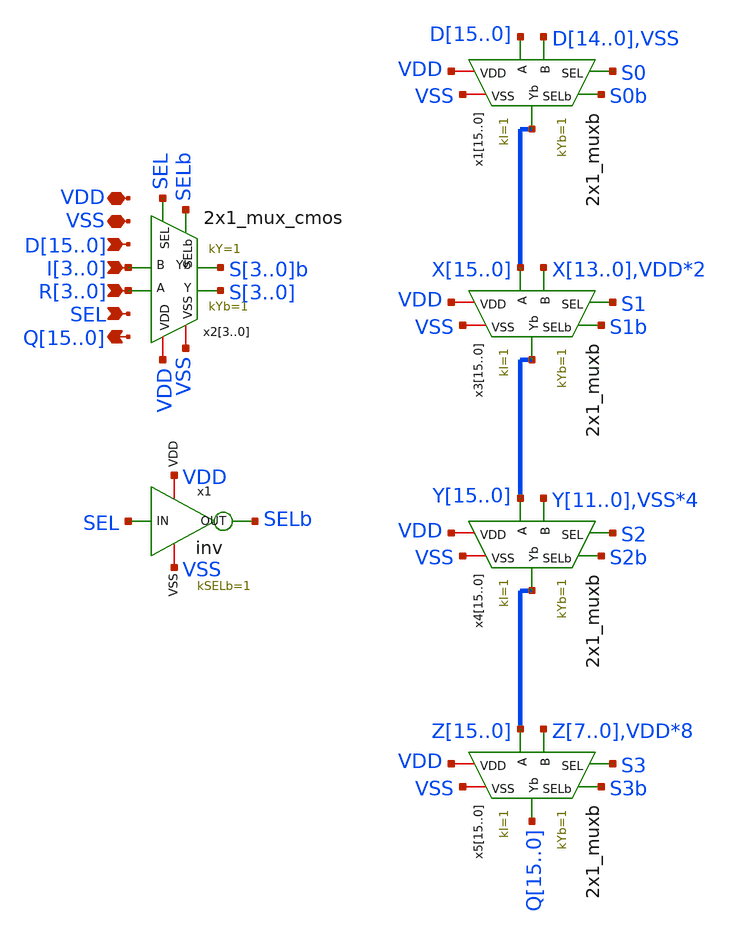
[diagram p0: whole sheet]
** sch_path: CAD5/shifter.sch
**.subckt shifter VDD VSS D15,D14,D13,D12,D11,D10,D9,D8,D7,D6,D5,D4,D3,D2,D1,D0
*+ Q15,Q14,Q13,Q12,Q11,Q10,Q9,Q8,Q7,Q6,Q5,Q4,Q3,Q2,Q1,Q0 R3,R2,R1,R0 I3,I2,I1,I0 SEL
*.iopin VDD
*.iopin VSS
*.ipin D15,D14,D13,D12,D11,D10,D9,D8,D7,D6,D5,D4,D3,D2,D1,D0
*.opin Q15,Q14,Q13,Q12,Q11,Q10,Q9,Q8,Q7,Q6,Q5,Q4,Q3,Q2,Q1,Q0
*.ipin R3,R2,R1,R0
*.ipin I3,I2,I1,I0
*.ipin SEL
x115 D15 S0 S0b VDD VSS D14 X15 2x1_muxb kI=1 kYb=1
x114 D14 S0 S0b VDD VSS D13 X14 2x1_muxb kI=1 kYb=1
x113 D13 S0 S0b VDD VSS D12 X13 2x1_muxb kI=1 kYb=1
x112 D12 S0 S0b VDD VSS D11 X12 2x1_muxb kI=1 kYb=1
x111 D11 S0 S0b VDD VSS D10 X11 2x1_muxb kI=1 kYb=1
x110 D10 S0 S0b VDD VSS D9 X10 2x1_muxb kI=1 kYb=1
x19 D9 S0 S0b VDD VSS D8 X9 2x1_muxb kI=1 kYb=1
x18 D8 S0 S0b VDD VSS D7 X8 2x1_muxb kI=1 kYb=1
x17 D7 S0 S0b VDD VSS D6 X7 2x1_muxb kI=1 kYb=1
x16 D6 S0 S0b VDD VSS D5 X6 2x1_muxb kI=1 kYb=1
x15 D5 S0 S0b VDD VSS D4 X5 2x1_muxb kI=1 kYb=1
x14 D4 S0 S0b VDD VSS D3 X4 2x1_muxb kI=1 kYb=1
x13 D3 S0 S0b VDD VSS D2 X3 2x1_muxb kI=1 kYb=1
x12 D2 S0 S0b VDD VSS D1 X2 2x1_muxb kI=1 kYb=1
x11 D1 S0 S0b VDD VSS D0 X1 2x1_muxb kI=1 kYb=1
x10 D0 S0 S0b VDD VSS VSS X0 2x1_muxb kI=1 kYb=1
x23 R3 SEL SELb S3 VDD VSS I3 S3b 2x1_mux_cmos kYb=1 kY=1
x22 R2 SEL SELb S2 VDD VSS I2 S2b 2x1_mux_cmos kYb=1 kY=1
x21 R1 SEL SELb S1 VDD VSS I1 S1b 2x1_mux_cmos kYb=1 kY=1
x20 R0 SEL SELb S0 VDD VSS I0 S0b 2x1_mux_cmos kYb=1 kY=1
x1 VDD SEL SELb VSS inv kSELb=1
x315 X15 S1 S1b VDD VSS X13 Y15 2x1_muxb kI=1 kYb=1
x314 X14 S1 S1b VDD VSS X12 Y14 2x1_muxb kI=1 kYb=1
x313 X13 S1 S1b VDD VSS X11 Y13 2x1_muxb kI=1 kYb=1
x312 X12 S1 S1b VDD VSS X10 Y12 2x1_muxb kI=1 kYb=1
x311 X11 S1 S1b VDD VSS X9 Y11 2x1_muxb kI=1 kYb=1
x310 X10 S1 S1b VDD VSS X8 Y10 2x1_muxb kI=1 kYb=1
x39 X9 S1 S1b VDD VSS X7 Y9 2x1_muxb kI=1 kYb=1
x38 X8 S1 S1b VDD VSS X6 Y8 2x1_muxb kI=1 kYb=1
x37 X7 S1 S1b VDD VSS X5 Y7 2x1_muxb kI=1 kYb=1
x36 X6 S1 S1b VDD VSS X4 Y6 2x1_muxb kI=1 kYb=1
x35 X5 S1 S1b VDD VSS X3 Y5 2x1_muxb kI=1 kYb=1
x34 X4 S1 S1b VDD VSS X2 Y4 2x1_muxb kI=1 kYb=1
x33 X3 S1 S1b VDD VSS X1 Y3 2x1_muxb kI=1 kYb=1
x32 X2 S1 S1b VDD VSS X0 Y2 2x1_muxb kI=1 kYb=1
x31 X1 S1 S1b VDD VSS VDD Y1 2x1_muxb kI=1 kYb=1
x30 X0 S1 S1b VDD VSS VDD Y0 2x1_muxb kI=1 kYb=1
x415 Y15 S2 S2b VDD VSS Y11 Z15 2x1_muxb kI=1 kYb=1
x414 Y14 S2 S2b VDD VSS Y10 Z14 2x1_muxb kI=1 kYb=1
x413 Y13 S2 S2b VDD VSS Y9 Z13 2x1_muxb kI=1 kYb=1
x412 Y12 S2 S2b VDD VSS Y8 Z12 2x1_muxb kI=1 kYb=1
x411 Y11 S2 S2b VDD VSS Y7 Z11 2x1_muxb kI=1 kYb=1
x410 Y10 S2 S2b VDD VSS Y6 Z10 2x1_muxb kI=1 kYb=1
x49 Y9 S2 S2b VDD VSS Y5 Z9 2x1_muxb kI=1 kYb=1
x48 Y8 S2 S2b VDD VSS Y4 Z8 2x1_muxb kI=1 kYb=1
x47 Y7 S2 S2b VDD VSS Y3 Z7 2x1_muxb kI=1 kYb=1
x46 Y6 S2 S2b VDD VSS Y2 Z6 2x1_muxb kI=1 kYb=1
x45 Y5 S2 S2b VDD VSS Y1 Z5 2x1_muxb kI=1 kYb=1
x44 Y4 S2 S2b VDD VSS Y0 Z4 2x1_muxb kI=1 kYb=1
x43 Y3 S2 S2b VDD VSS VSS Z3 2x1_muxb kI=1 kYb=1
x42 Y2 S2 S2b VDD VSS VSS Z2 2x1_muxb kI=1 kYb=1
x41 Y1 S2 S2b VDD VSS VSS Z1 2x1_muxb kI=1 kYb=1
x40 Y0 S2 S2b VDD VSS VSS Z0 2x1_muxb kI=1 kYb=1
x515 Z15 S3 S3b VDD VSS Z7 Q15 2x1_muxb kI=1 kYb=1
x514 Z14 S3 S3b VDD VSS Z6 Q14 2x1_muxb kI=1 kYb=1
x513 Z13 S3 S3b VDD VSS Z5 Q13 2x1_muxb kI=1 kYb=1
x512 Z12 S3 S3b VDD VSS Z4 Q12 2x1_muxb kI=1 kYb=1
x511 Z11 S3 S3b VDD VSS Z3 Q11 2x1_muxb kI=1 kYb=1
x510 Z10 S3 S3b VDD VSS Z2 Q10 2x1_muxb kI=1 kYb=1
x59 Z9 S3 S3b VDD VSS Z1 Q9 2x1_muxb kI=1 kYb=1
x58 Z8 S3 S3b VDD VSS Z0 Q8 2x1_muxb kI=1 kYb=1
x57 Z7 S3 S3b VDD VSS VDD Q7 2x1_muxb kI=1 kYb=1
x56 Z6 S3 S3b VDD VSS VDD Q6 2x1_muxb kI=1 kYb=1
x55 Z5 S3 S3b VDD VSS VDD Q5 2x1_muxb kI=1 kYb=1
x54 Z4 S3 S3b VDD VSS VDD Q4 2x1_muxb kI=1 kYb=1
x53 Z3 S3 S3b VDD VSS VDD Q3 2x1_muxb kI=1 kYb=1
x52 Z2 S3 S3b VDD VSS VDD Q2 2x1_muxb kI=1 kYb=1
x51 Z1 S3 S3b VDD VSS VDD Q1 2x1_muxb kI=1 kYb=1
x50 Z0 S3 S3b VDD VSS VDD Q0 2x1_muxb kI=1 kYb=1
**.ends

* expanding   symbol:  engn1600-team1/CAD5/2x1_muxb.sym # of pins=7
** sym_path: CAD5/2x1_muxb.sym
** sch_path: CAD5/2x1_muxb.sch
.subckt 2x1_muxb A SEL SELb VDD VSS B Yb  kI=1 kYb=1
*.ipin A
*.ipin B
*.ipin SEL
*.iopin VDD
*.iopin VSS
*.ipin SELb
*.opin Yb
XM1 VSS B net1 VSS nfet_03v3 L=0.28u W='kI*0.36u' nf=1 ad='int((nf+1)/2) * W/nf * 0.18u' as='int((nf+2)/2) * W/nf * 0.18u'
+ pd='2*int((nf+1)/2) * (W/nf + 0.18u)' ps='2*int((nf+2)/2) * (W/nf + 0.18u)' nrd='0.18u / W' nrs='0.18u / W'
+ sa=0 sb=0 sd=0 m=1
XM2 net1 SEL Yb VSS nfet_03v3 L=0.28u W='kYb*0.36u' nf=1 ad='int((nf+1)/2) * W/nf * 0.18u' as='int((nf+2)/2) * W/nf * 0.18u'
+ pd='2*int((nf+1)/2) * (W/nf + 0.18u)' ps='2*int((nf+2)/2) * (W/nf + 0.18u)' nrd='0.18u / W' nrs='0.18u / W'
+ sa=0 sb=0 sd=0 m=1
XM3 Yb SELb net2 VSS nfet_03v3 L=0.28u W='kYb*0.36u' nf=1 ad='int((nf+1)/2) * W/nf * 0.18u' as='int((nf+2)/2) * W/nf * 0.18u'
+ pd='2*int((nf+1)/2) * (W/nf + 0.18u)' ps='2*int((nf+2)/2) * (W/nf + 0.18u)' nrd='0.18u / W' nrs='0.18u / W'
+ sa=0 sb=0 sd=0 m=1
XM4 net2 A VSS VSS nfet_03v3 L=0.28u W='kI*0.36u' nf=1 ad='int((nf+1)/2) * W/nf * 0.18u' as='int((nf+2)/2) * W/nf * 0.18u'
+ pd='2*int((nf+1)/2) * (W/nf + 0.18u)' ps='2*int((nf+2)/2) * (W/nf + 0.18u)' nrd='0.18u / W' nrs='0.18u / W'
+ sa=0 sb=0 sd=0 m=1
XM5 net3 SELb Yb VDD pfet_03v3 L=0.28u W='kYb*0.72u' nf=1 ad='int((nf+1)/2) * W/nf * 0.18u' as='int((nf+2)/2) * W/nf * 0.18u'
+ pd='2*int((nf+1)/2) * (W/nf + 0.18u)' ps='2*int((nf+2)/2) * (W/nf + 0.18u)' nrd='0.18u / W' nrs='0.18u / W'
+ sa=0 sb=0 sd=0 m=1
XM6 VDD B net3 VDD pfet_03v3 L=0.28u W='kI*0.72u' nf=1 ad='int((nf+1)/2) * W/nf * 0.18u' as='int((nf+2)/2) * W/nf * 0.18u'
+ pd='2*int((nf+1)/2) * (W/nf + 0.18u)' ps='2*int((nf+2)/2) * (W/nf + 0.18u)' nrd='0.18u / W' nrs='0.18u / W'
+ sa=0 sb=0 sd=0 m=1
XM7 net4 A VDD VDD pfet_03v3 L=0.28u W='kI*0.72u' nf=1 ad='int((nf+1)/2) * W/nf * 0.18u' as='int((nf+2)/2) * W/nf * 0.18u'
+ pd='2*int((nf+1)/2) * (W/nf + 0.18u)' ps='2*int((nf+2)/2) * (W/nf + 0.18u)' nrd='0.18u / W' nrs='0.18u / W'
+ sa=0 sb=0 sd=0 m=1
XM8 Yb SEL net4 VDD pfet_03v3 L=0.28u W='kYb*0.72u' nf=1 ad='int((nf+1)/2) * W/nf * 0.18u' as='int((nf+2)/2) * W/nf * 0.18u'
+ pd='2*int((nf+1)/2) * (W/nf + 0.18u)' ps='2*int((nf+2)/2) * (W/nf + 0.18u)' nrd='0.18u / W' nrs='0.18u / W'
+ sa=0 sb=0 sd=0 m=1
**** begin user architecture code


.param kI=1
.param kYb=1


**** end user architecture code
.ends


* expanding   symbol:  engn1600-team1/CAD5/2x1_mux_cmos.sym # of pins=8
** sym_path: CAD4/2x1_mux_cmos.sym
** sch_path: CAD4/2x1_mux_cmos.sch
.subckt 2x1_mux_cmos A SEL SELb Y VDD VSS B Yb  kYb=1 kY=1
*.ipin A
*.ipin B
*.ipin SEL
*.opin Y
*.iopin VDD
*.iopin VSS
*.ipin SELb
*.opin Yb
XM1 VSS B net1 VSS nfet_03v3 L=0.28u W='kI*0.36u' nf=1 ad='int((nf+1)/2) * W/nf * 0.18u' as='int((nf+2)/2) * W/nf * 0.18u'
+ pd='2*int((nf+1)/2) * (W/nf + 0.18u)' ps='2*int((nf+2)/2) * (W/nf + 0.18u)' nrd='0.18u / W' nrs='0.18u / W'
+ sa=0 sb=0 sd=0 m=1
XM2 net1 SEL Yb VSS nfet_03v3 L=0.28u W='kYb*0.36u' nf=1 ad='int((nf+1)/2) * W/nf * 0.18u' as='int((nf+2)/2) * W/nf * 0.18u'
+ pd='2*int((nf+1)/2) * (W/nf + 0.18u)' ps='2*int((nf+2)/2) * (W/nf + 0.18u)' nrd='0.18u / W' nrs='0.18u / W'
+ sa=0 sb=0 sd=0 m=1
XM3 Yb SELb net2 VSS nfet_03v3 L=0.28u W='kYb*0.36u' nf=1 ad='int((nf+1)/2) * W/nf * 0.18u' as='int((nf+2)/2) * W/nf * 0.18u'
+ pd='2*int((nf+1)/2) * (W/nf + 0.18u)' ps='2*int((nf+2)/2) * (W/nf + 0.18u)' nrd='0.18u / W' nrs='0.18u / W'
+ sa=0 sb=0 sd=0 m=1
XM4 net2 A VSS VSS nfet_03v3 L=0.28u W='kI*0.36u' nf=1 ad='int((nf+1)/2) * W/nf * 0.18u' as='int((nf+2)/2) * W/nf * 0.18u'
+ pd='2*int((nf+1)/2) * (W/nf + 0.18u)' ps='2*int((nf+2)/2) * (W/nf + 0.18u)' nrd='0.18u / W' nrs='0.18u / W'
+ sa=0 sb=0 sd=0 m=1
XM5 net3 SELb Yb VDD pfet_03v3 L=0.28u W='kYb*0.72u' nf=1 ad='int((nf+1)/2) * W/nf * 0.18u' as='int((nf+2)/2) * W/nf * 0.18u'
+ pd='2*int((nf+1)/2) * (W/nf + 0.18u)' ps='2*int((nf+2)/2) * (W/nf + 0.18u)' nrd='0.18u / W' nrs='0.18u / W'
+ sa=0 sb=0 sd=0 m=1
XM6 VDD B net3 VDD pfet_03v3 L=0.28u W='kI*0.72u' nf=1 ad='int((nf+1)/2) * W/nf * 0.18u' as='int((nf+2)/2) * W/nf * 0.18u'
+ pd='2*int((nf+1)/2) * (W/nf + 0.18u)' ps='2*int((nf+2)/2) * (W/nf + 0.18u)' nrd='0.18u / W' nrs='0.18u / W'
+ sa=0 sb=0 sd=0 m=1
XM7 net4 A VDD VDD pfet_03v3 L=0.28u W='kI*0.72u' nf=1 ad='int((nf+1)/2) * W/nf * 0.18u' as='int((nf+2)/2) * W/nf * 0.18u'
+ pd='2*int((nf+1)/2) * (W/nf + 0.18u)' ps='2*int((nf+2)/2) * (W/nf + 0.18u)' nrd='0.18u / W' nrs='0.18u / W'
+ sa=0 sb=0 sd=0 m=1
XM8 Yb SEL net4 VDD pfet_03v3 L=0.28u W='kYb*0.72u' nf=1 ad='int((nf+1)/2) * W/nf * 0.18u' as='int((nf+2)/2) * W/nf * 0.18u'
+ pd='2*int((nf+1)/2) * (W/nf + 0.18u)' ps='2*int((nf+2)/2) * (W/nf + 0.18u)' nrd='0.18u / W' nrs='0.18u / W'
+ sa=0 sb=0 sd=0 m=1
XM9 VSS Yb Y VSS nfet_03v3 L=0.28u W='kY*0.36u' nf=1 ad='int((nf+1)/2) * W/nf * 0.18u' as='int((nf+2)/2) * W/nf * 0.18u'
+ pd='2*int((nf+1)/2) * (W/nf + 0.18u)' ps='2*int((nf+2)/2) * (W/nf + 0.18u)' nrd='0.18u / W' nrs='0.18u / W'
+ sa=0 sb=0 sd=0 m=1
XM10 VDD Yb Y VDD pfet_03v3 L=0.28u W='kY*0.72u' nf=1 ad='int((nf+1)/2) * W/nf * 0.18u' as='int((nf+2)/2) * W/nf * 0.18u'
+ pd='2*int((nf+1)/2) * (W/nf + 0.18u)' ps='2*int((nf+2)/2) * (W/nf + 0.18u)' nrd='0.18u / W' nrs='0.18u / W'
+ sa=0 sb=0 sd=0 m=1
**** begin user architecture code


.param kI=2.5
.param kYb=1.875
.param kY=2.1527777777777778


**** end user architecture code
.ends


* expanding   symbol:  engn1600-team1/CAD5/inv.sym # of pins=4
** sym_path: CAD5/inv.sym
** sch_path: CAD5/inv.sch
.subckt inv VDD IN OUT VSS  kSELb=1
*.ipin IN
*.opin OUT
*.iopin VDD
*.iopin VSS
XM1 OUT IN VDD VDD pfet_03v3 L=0.28u W='kSELb*0.72u' nf=1 ad='int((nf+1)/2) * W/nf * 0.18u' as='int((nf+2)/2) * W/nf * 0.18u'
+ pd='2*int((nf+1)/2) * (W/nf + 0.18u)' ps='2*int((nf+2)/2) * (W/nf + 0.18u)' nrd='0.18u / W' nrs='0.18u / W'
+ sa=0 sb=0 sd=0 m=1
XM2 OUT IN VSS VSS nfet_03v3 L=0.28u W='kSELb*0.36u' nf=1 ad='int((nf+1)/2) * W/nf * 0.18u' as='int((nf+2)/2) * W/nf * 0.18u'
+ pd='2*int((nf+1)/2) * (W/nf + 0.18u)' ps='2*int((nf+2)/2) * (W/nf + 0.18u)' nrd='0.18u / W' nrs='0.18u / W'
+ sa=0 sb=0 sd=0 m=1
**** begin user architecture code


.param kSELb=1


**** end user architecture code
.ends

.end
